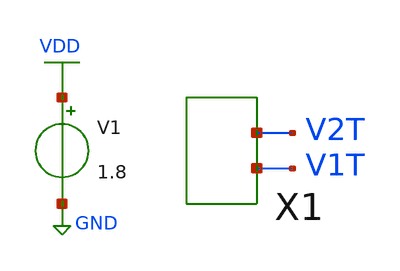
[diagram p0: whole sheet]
** sch_path: xschem/vdiv_tb.sch
**.subckt vdiv_tb
X1 V1T V2T vdiv
V1 VDD GND 1.8
.save i(v1)
**** begin user architecture code


.option wnflag=1
.lib /usr/local/share/pdk/sky130A/libs.tech/ngspice/sky130.lib.spice tt
.op
.save all


**** end user architecture code
**.ends

* expanding   symbol:  vdiv.sym # of pins=2
** sym_path: xschem/vdiv.sym
** sch_path: xschem/vdiv.sch
.subckt vdiv v1t v2t
*.iopin v2t
*.iopin v1t
XR1 v2t VDD res100k
XR2 v1t v2t res100k
XR3 GND v1t res100k
.ends


* expanding   symbol:  res100k.sym # of pins=2
** sym_path: xschem/res100k.sym
** sch_path: xschem/res100k.sch
.subckt res100k bot top
*.iopin top
*.iopin bot
XR1 net1 top GND sky130_fd_pr__res_xhigh_po W=0.35 L=3.5 mult=1 m=1
XR2 net2 net1 GND sky130_fd_pr__res_xhigh_po W=0.35 L=3.5 mult=1 m=1
XR3 net3 net2 GND sky130_fd_pr__res_xhigh_po W=0.35 L=3.5 mult=1 m=1
XR4 net4 net3 GND sky130_fd_pr__res_xhigh_po W=0.35 L=3.5 mult=1 m=1
XR5 bot net4 GND sky130_fd_pr__res_xhigh_po W=0.35 L=3.5 mult=1 m=1
.ends

.GLOBAL GND
.GLOBAL VDD
.end
